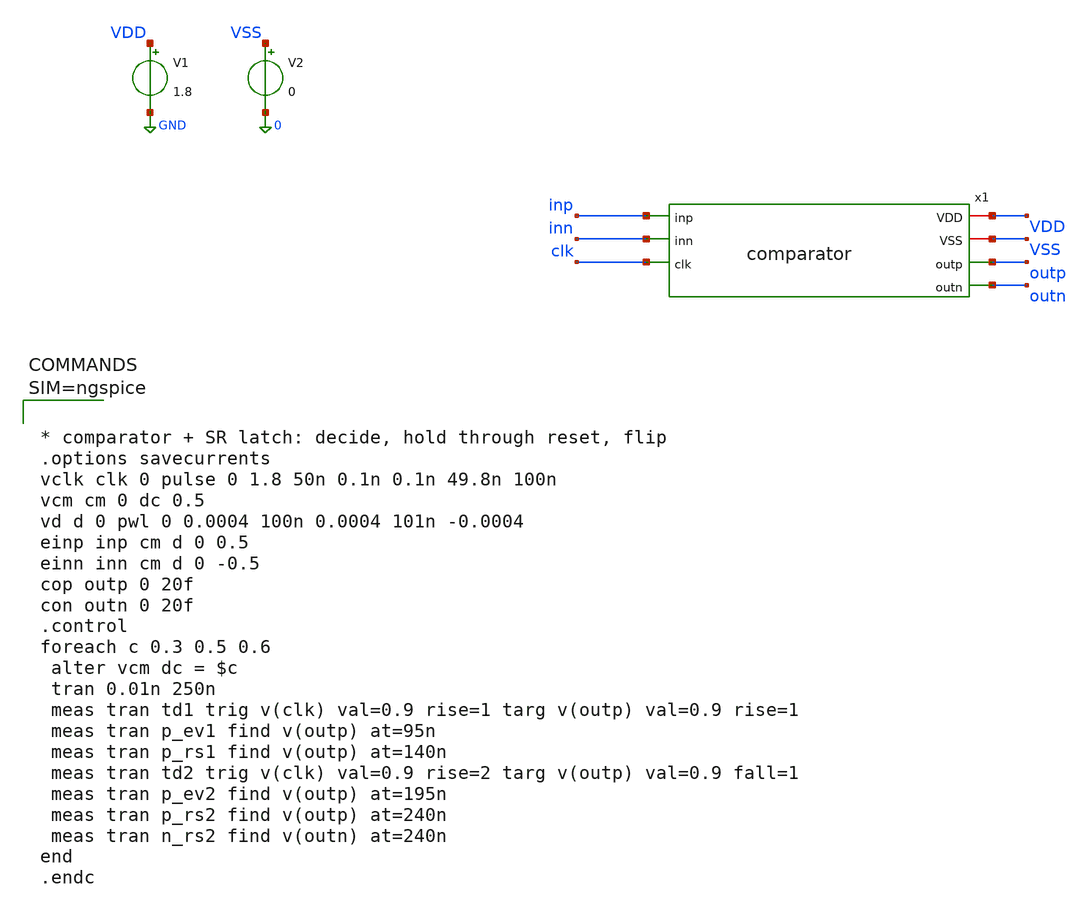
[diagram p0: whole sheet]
** sch_path: xschem/comparator_tb.sch
**.subckt comparator_tb
V1 VDD GND 1.8
V2 VSS 0 0
x1 inp VDD inn clk VSS outp outn comparator
**** begin user architecture code

** opencircuitdesign pdks install
.lib $::SKYWATER_MODELS/sky130.lib.spice tt




* comparator + SR latch: decide, hold through reset, flip
.options savecurrents
vclk clk 0 pulse 0 1.8 50n 0.1n 0.1n 49.8n 100n
vcm cm 0 dc 0.5
vd d 0 pwl 0 0.0004 100n 0.0004 101n -0.0004
einp inp cm d 0 0.5
einn inn cm d 0 -0.5
cop outp 0 20f
con outn 0 20f
.control
foreach c 0.3 0.5 0.6
 alter vcm dc = $c
 tran 0.01n 250n
 meas tran td1 trig v(clk) val=0.9 rise=1 targ v(outp) val=0.9 rise=1
 meas tran p_ev1 find v(outp) at=95n
 meas tran p_rs1 find v(outp) at=140n
 meas tran td2 trig v(clk) val=0.9 rise=2 targ v(outp) val=0.9 fall=1
 meas tran p_ev2 find v(outp) at=195n
 meas tran p_rs2 find v(outp) at=240n
 meas tran n_rs2 find v(outn) at=240n
end
.endc



**** end user architecture code
**.ends

* expanding   symbol:  comparator.sym # of pins=7
** sym_path: xschem/comparator.sym
** sch_path: xschem/comparator.sch
.subckt comparator inp VDD inn clk VSS outp outn
*.ipin inp
*.ipin inn
*.ipin clk
*.opin outp
*.opin outn
*.iopin VDD
*.iopin VSS
x1 inp VDD inn clk VSS X Y comparator_sa
XMI1N Yb Y VSS VSS sky130_fd_pr__nfet_01v8 L=0.15 W=1 nf=1 ad='int((1 + 1)/2) * 1 / 1 * 0.29' as='int((1 + 2)/2) * 1 / 1 * 0.29'
+ pd='2*int((1 + 1)/2) * (1 / 1 + 0.29)' ps='2*int((1 + 2)/2) * (1 / 1 + 0.29)' nrd='0.29 / 1 ' nrs='0.29 / 1 '
+ sa=0 sb=0 sd=0 mult=1 m=1
XMI1P Yb Y VDD VDD sky130_fd_pr__pfet_01v8 L=0.15 W=2 nf=1 ad='int((1 + 1)/2) * 2 / 1 * 0.29' as='int((1 + 2)/2) * 2 / 1 * 0.29'
+ pd='2*int((1 + 1)/2) * (2 / 1 + 0.29)' ps='2*int((1 + 2)/2) * (2 / 1 + 0.29)' nrd='0.29 / 2 ' nrs='0.29 / 2 '
+ sa=0 sb=0 sd=0 mult=1 m=1
XMI2N Xb X VSS VSS sky130_fd_pr__nfet_01v8 L=0.15 W=1 nf=1 ad='int((1 + 1)/2) * 1 / 1 * 0.29' as='int((1 + 2)/2) * 1 / 1 * 0.29'
+ pd='2*int((1 + 1)/2) * (1 / 1 + 0.29)' ps='2*int((1 + 2)/2) * (1 / 1 + 0.29)' nrd='0.29 / 1 ' nrs='0.29 / 1 '
+ sa=0 sb=0 sd=0 mult=1 m=1
XMI2P Xb X VDD VDD sky130_fd_pr__pfet_01v8 L=0.15 W=2 nf=1 ad='int((1 + 1)/2) * 2 / 1 * 0.29' as='int((1 + 2)/2) * 2 / 1 * 0.29'
+ pd='2*int((1 + 1)/2) * (2 / 1 + 0.29)' ps='2*int((1 + 2)/2) * (2 / 1 + 0.29)' nrd='0.29 / 2 ' nrs='0.29 / 2 '
+ sa=0 sb=0 sd=0 mult=1 m=1
XMA1 outp Yb VDD VDD sky130_fd_pr__pfet_01v8 L=0.15 W=1 nf=1 ad='int((1 + 1)/2) * 1 / 1 * 0.29' as='int((1 + 2)/2) * 1 / 1 * 0.29'
+ pd='2*int((1 + 1)/2) * (1 / 1 + 0.29)' ps='2*int((1 + 2)/2) * (1 / 1 + 0.29)' nrd='0.29 / 1 ' nrs='0.29 / 1 '
+ sa=0 sb=0 sd=0 mult=1 m=1
XMA2 outp outn VDD VDD sky130_fd_pr__pfet_01v8 L=0.15 W=1 nf=1 ad='int((1 + 1)/2) * 1 / 1 * 0.29' as='int((1 + 2)/2) * 1 / 1 * 0.29'
+ pd='2*int((1 + 1)/2) * (1 / 1 + 0.29)' ps='2*int((1 + 2)/2) * (1 / 1 + 0.29)' nrd='0.29 / 1 ' nrs='0.29 / 1 '
+ sa=0 sb=0 sd=0 mult=1 m=1
XMA3 outp Yb na VSS sky130_fd_pr__nfet_01v8 L=0.15 W=2 nf=1 ad='int((1 + 1)/2) * 2 / 1 * 0.29' as='int((1 + 2)/2) * 2 / 1 * 0.29'
+ pd='2*int((1 + 1)/2) * (2 / 1 + 0.29)' ps='2*int((1 + 2)/2) * (2 / 1 + 0.29)' nrd='0.29 / 2 ' nrs='0.29 / 2 '
+ sa=0 sb=0 sd=0 mult=1 m=1
XMA4 na outn VSS VSS sky130_fd_pr__nfet_01v8 L=0.15 W=2 nf=1 ad='int((1 + 1)/2) * 2 / 1 * 0.29' as='int((1 + 2)/2) * 2 / 1 * 0.29'
+ pd='2*int((1 + 1)/2) * (2 / 1 + 0.29)' ps='2*int((1 + 2)/2) * (2 / 1 + 0.29)' nrd='0.29 / 2 ' nrs='0.29 / 2 '
+ sa=0 sb=0 sd=0 mult=1 m=1
XMB1 outn Xb VDD VDD sky130_fd_pr__pfet_01v8 L=0.15 W=1 nf=1 ad='int((1 + 1)/2) * 1 / 1 * 0.29' as='int((1 + 2)/2) * 1 / 1 * 0.29'
+ pd='2*int((1 + 1)/2) * (1 / 1 + 0.29)' ps='2*int((1 + 2)/2) * (1 / 1 + 0.29)' nrd='0.29 / 1 ' nrs='0.29 / 1 '
+ sa=0 sb=0 sd=0 mult=1 m=1
XMB2 outn outp VDD VDD sky130_fd_pr__pfet_01v8 L=0.15 W=1 nf=1 ad='int((1 + 1)/2) * 1 / 1 * 0.29' as='int((1 + 2)/2) * 1 / 1 * 0.29'
+ pd='2*int((1 + 1)/2) * (1 / 1 + 0.29)' ps='2*int((1 + 2)/2) * (1 / 1 + 0.29)' nrd='0.29 / 1 ' nrs='0.29 / 1 '
+ sa=0 sb=0 sd=0 mult=1 m=1
XMB3 outn Xb nb VSS sky130_fd_pr__nfet_01v8 L=0.15 W=2 nf=1 ad='int((1 + 1)/2) * 2 / 1 * 0.29' as='int((1 + 2)/2) * 2 / 1 * 0.29'
+ pd='2*int((1 + 1)/2) * (2 / 1 + 0.29)' ps='2*int((1 + 2)/2) * (2 / 1 + 0.29)' nrd='0.29 / 2 ' nrs='0.29 / 2 '
+ sa=0 sb=0 sd=0 mult=1 m=1
XMB4 nb outp VSS VSS sky130_fd_pr__nfet_01v8 L=0.15 W=2 nf=1 ad='int((1 + 1)/2) * 2 / 1 * 0.29' as='int((1 + 2)/2) * 2 / 1 * 0.29'
+ pd='2*int((1 + 1)/2) * (2 / 1 + 0.29)' ps='2*int((1 + 2)/2) * (2 / 1 + 0.29)' nrd='0.29 / 2 ' nrs='0.29 / 2 '
+ sa=0 sb=0 sd=0 mult=1 m=1
.ends


* expanding   symbol:  comparator_sa.sym # of pins=7
** sym_path: xschem/comparator_sa.sym
** sch_path: xschem/comparator_sa.sch
.subckt comparator_sa inp VDD inn clk VSS X Y
*.ipin inp
*.ipin inn
*.ipin clk
*.opin X
*.opin Y
*.iopin VDD
*.iopin VSS
XM7 T ckb VDD VDD sky130_fd_pr__pfet_01v8 L=0.15 W=4 nf=1 ad='int((1 + 1)/2) * 4 / 1 * 0.29' as='int((1 + 2)/2) * 4 / 1 * 0.29'
+ pd='2*int((1 + 1)/2) * (4 / 1 + 0.29)' ps='2*int((1 + 2)/2) * (4 / 1 + 0.29)' nrd='0.29 / 4 ' nrs='0.29 / 4 '
+ sa=0 sb=0 sd=0 mult=1 m=1
XM1 P inp T T sky130_fd_pr__pfet_01v8 L=0.5 W=8 nf=4 ad='int((4 + 1)/2) * 8 / 4 * 0.29' as='int((4 + 2)/2) * 8 / 4 * 0.29'
+ pd='2*int((4 + 1)/2) * (8 / 4 + 0.29)' ps='2*int((4 + 2)/2) * (8 / 4 + 0.29)' nrd='0.29 / 8 ' nrs='0.29 / 8 '
+ sa=0 sb=0 sd=0 mult=1 m=1
XM2 Q inn T T sky130_fd_pr__pfet_01v8 L=0.5 W=8 nf=4 ad='int((4 + 1)/2) * 8 / 4 * 0.29' as='int((4 + 2)/2) * 8 / 4 * 0.29'
+ pd='2*int((4 + 1)/2) * (8 / 4 + 0.29)' ps='2*int((4 + 2)/2) * (8 / 4 + 0.29)' nrd='0.29 / 8 ' nrs='0.29 / 8 '
+ sa=0 sb=0 sd=0 mult=1 m=1
XM3 X Y P VDD sky130_fd_pr__pfet_01v8 L=0.15 W=2 nf=1 ad='int((1 + 1)/2) * 2 / 1 * 0.29' as='int((1 + 2)/2) * 2 / 1 * 0.29'
+ pd='2*int((1 + 1)/2) * (2 / 1 + 0.29)' ps='2*int((1 + 2)/2) * (2 / 1 + 0.29)' nrd='0.29 / 2 ' nrs='0.29 / 2 '
+ sa=0 sb=0 sd=0 mult=1 m=1
XM4 Y X Q VDD sky130_fd_pr__pfet_01v8 L=0.15 W=2 nf=1 ad='int((1 + 1)/2) * 2 / 1 * 0.29' as='int((1 + 2)/2) * 2 / 1 * 0.29'
+ pd='2*int((1 + 1)/2) * (2 / 1 + 0.29)' ps='2*int((1 + 2)/2) * (2 / 1 + 0.29)' nrd='0.29 / 2 ' nrs='0.29 / 2 '
+ sa=0 sb=0 sd=0 mult=1 m=1
XM6 Y X VSS VSS sky130_fd_pr__nfet_01v8 L=0.15 W=1 nf=1 ad='int((1 + 1)/2) * 1 / 1 * 0.29' as='int((1 + 2)/2) * 1 / 1 * 0.29'
+ pd='2*int((1 + 1)/2) * (1 / 1 + 0.29)' ps='2*int((1 + 2)/2) * (1 / 1 + 0.29)' nrd='0.29 / 1 ' nrs='0.29 / 1 '
+ sa=0 sb=0 sd=0 mult=1 m=1
XM5 X Y VSS VSS sky130_fd_pr__nfet_01v8 L=0.15 W=1 nf=1 ad='int((1 + 1)/2) * 1 / 1 * 0.29' as='int((1 + 2)/2) * 1 / 1 * 0.29'
+ pd='2*int((1 + 1)/2) * (1 / 1 + 0.29)' ps='2*int((1 + 2)/2) * (1 / 1 + 0.29)' nrd='0.29 / 1 ' nrs='0.29 / 1 '
+ sa=0 sb=0 sd=0 mult=1 m=1
XS4 Y ckb VSS VSS sky130_fd_pr__nfet_01v8 L=0.6 W=2 nf=1 ad='int((1 + 1)/2) * 2 / 1 * 0.29' as='int((1 + 2)/2) * 2 / 1 * 0.29'
+ pd='2*int((1 + 1)/2) * (2 / 1 + 0.29)' ps='2*int((1 + 2)/2) * (2 / 1 + 0.29)' nrd='0.29 / 2 ' nrs='0.29 / 2 '
+ sa=0 sb=0 sd=0 mult=1 m=1
XS2 Q ckb VSS VSS sky130_fd_pr__nfet_01v8 L=0.6 W=2 nf=1 ad='int((1 + 1)/2) * 2 / 1 * 0.29' as='int((1 + 2)/2) * 2 / 1 * 0.29'
+ pd='2*int((1 + 1)/2) * (2 / 1 + 0.29)' ps='2*int((1 + 2)/2) * (2 / 1 + 0.29)' nrd='0.29 / 2 ' nrs='0.29 / 2 '
+ sa=0 sb=0 sd=0 mult=1 m=1
XS3 X ckb VSS VSS sky130_fd_pr__nfet_01v8 L=0.6 W=2 nf=1 ad='int((1 + 1)/2) * 2 / 1 * 0.29' as='int((1 + 2)/2) * 2 / 1 * 0.29'
+ pd='2*int((1 + 1)/2) * (2 / 1 + 0.29)' ps='2*int((1 + 2)/2) * (2 / 1 + 0.29)' nrd='0.29 / 2 ' nrs='0.29 / 2 '
+ sa=0 sb=0 sd=0 mult=1 m=1
XS1 P ckb VSS VSS sky130_fd_pr__nfet_01v8 L=0.6 W=2 nf=1 ad='int((1 + 1)/2) * 2 / 1 * 0.29' as='int((1 + 2)/2) * 2 / 1 * 0.29'
+ pd='2*int((1 + 1)/2) * (2 / 1 + 0.29)' ps='2*int((1 + 2)/2) * (2 / 1 + 0.29)' nrd='0.29 / 2 ' nrs='0.29 / 2 '
+ sa=0 sb=0 sd=0 mult=1 m=1
XMIN ckb clk VSS VSS sky130_fd_pr__nfet_01v8 L=0.15 W=1 nf=1 ad='int((1 + 1)/2) * 1 / 1 * 0.29' as='int((1 + 2)/2) * 1 / 1 * 0.29'
+ pd='2*int((1 + 1)/2) * (1 / 1 + 0.29)' ps='2*int((1 + 2)/2) * (1 / 1 + 0.29)' nrd='0.29 / 1 ' nrs='0.29 / 1 '
+ sa=0 sb=0 sd=0 mult=1 m=1
XMIP ckb clk VDD VDD sky130_fd_pr__pfet_01v8 L=0.15 W=2 nf=1 ad='int((1 + 1)/2) * 2 / 1 * 0.29' as='int((1 + 2)/2) * 2 / 1 * 0.29'
+ pd='2*int((1 + 1)/2) * (2 / 1 + 0.29)' ps='2*int((1 + 2)/2) * (2 / 1 + 0.29)' nrd='0.29 / 2 ' nrs='0.29 / 2 '
+ sa=0 sb=0 sd=0 mult=1 m=1
.ends

.GLOBAL GND
.end
